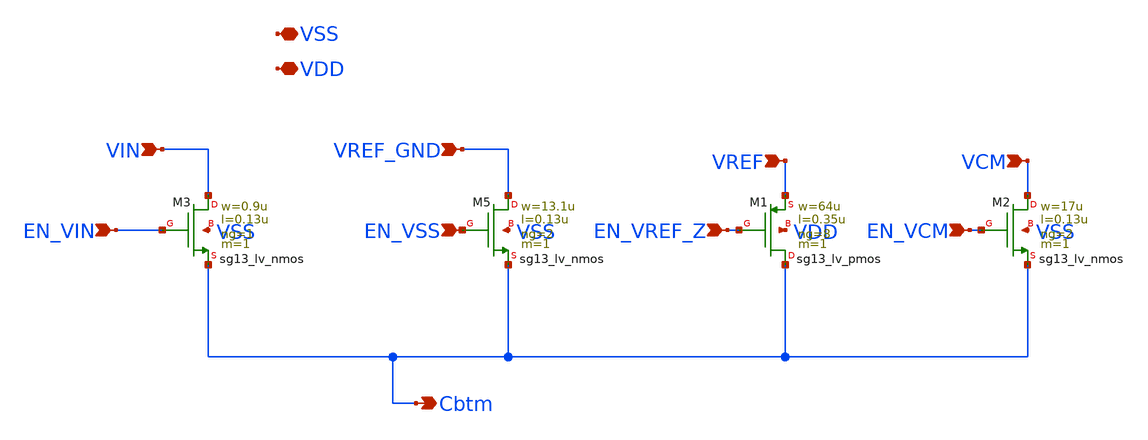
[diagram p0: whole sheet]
** sch_path: schematic/individual_switches/switch_C9.sch
**.subckt switch_C9 VIN EN_VIN VREF_GND EN_VSS Cbtm VSS VREF EN_VREF_Z EN_VCM VCM VDD
*.ipin VIN
*.ipin EN_VIN
*.ipin VREF_GND
*.ipin EN_VSS
*.opin Cbtm
*.iopin VSS
*.ipin VREF
*.ipin EN_VREF_Z
*.ipin EN_VCM
*.ipin VCM
*.iopin VDD
XM3 VIN EN_VIN Cbtm VSS sg13_lv_nmos w=0.9u l=0.13u ng=1 m=1 mm_ok=1
XM5 VREF_GND EN_VSS Cbtm VSS sg13_lv_nmos w=13.1u l=0.13u ng=2 m=1 mm_ok=1
XM1 Cbtm EN_VREF_Z VREF VDD sg13_lv_pmos w=64u l=0.35u ng=8 m=1 mm_ok=1
XM2 VCM EN_VCM Cbtm VSS sg13_lv_nmos w=17u l=0.13u ng=2 m=1 mm_ok=1
**.ends
.end
